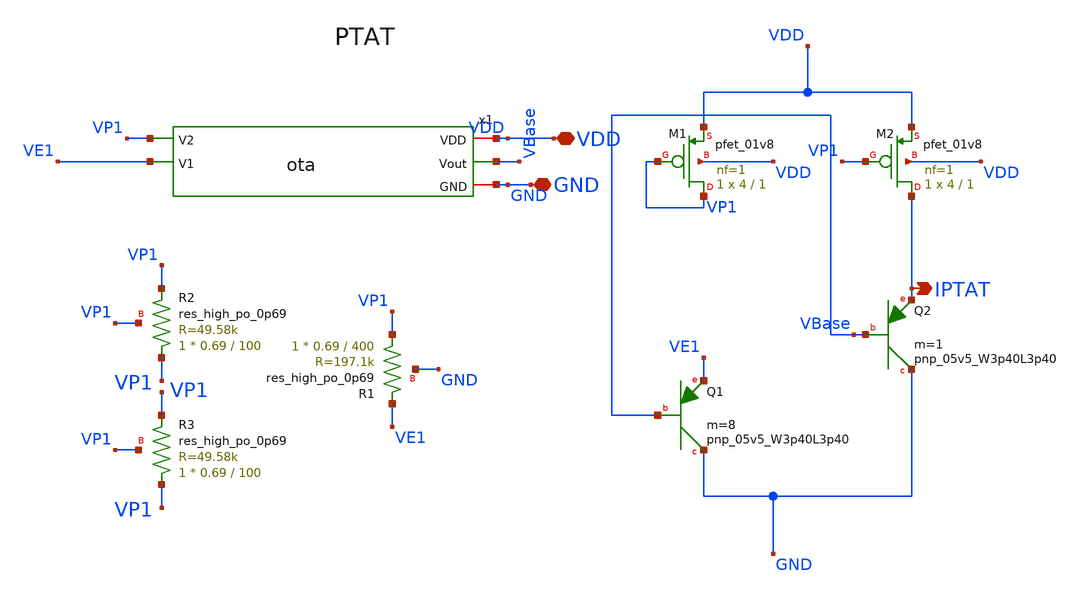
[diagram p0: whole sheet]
** sch_path: subcells/xschem/ptat.sch
**.subckt ptat VDD GND IPTAT
*.iopin VDD
*.iopin GND
*.opin IPTAT
XM1 VP1 VP1 VDD VDD sky130_fd_pr__pfet_01v8 L=1 W=4 nf=1 ad='int((1 + 1)/2) * 4 / 1 * 0.29' as='int((1 + 2)/2) * 4 / 1 * 0.29'
+ pd='2*int((1 + 1)/2) * (4 / 1 + 0.29)' ps='2*int((1 + 2)/2) * (4 / 1 + 0.29)' nrd='0.29 / 4 ' nrs='0.29 / 4 '
+ sa=0 sb=0 sd=0 mult=1 m=1
XM2 IPTAT VP1 VDD VDD sky130_fd_pr__pfet_01v8 L=1 W=4 nf=1 ad='int((1 + 1)/2) * 4 / 1 * 0.29' as='int((1 + 2)/2) * 4 / 1 * 0.29'
+ pd='2*int((1 + 1)/2) * (4 / 1 + 0.29)' ps='2*int((1 + 2)/2) * (4 / 1 + 0.29)' nrd='0.29 / 4 ' nrs='0.29 / 4 '
+ sa=0 sb=0 sd=0 mult=1 m=1
XR1 VP1 VE1 GND sky130_fd_pr__res_high_po_0p69 L=400 mult=1 m=1
x1 VDD VP1 VE1 VBase GND ota
XQ1 GND VBase VE1 sky130_fd_pr__pnp_05v5_W3p40L3p40 m=8
XQ2 GND VBase IPTAT sky130_fd_pr__pnp_05v5_W3p40L3p40 m=1
XR2 VP1 VP1 VP1 sky130_fd_pr__res_high_po_0p69 L=100 mult=1 m=1
XR3 VP1 VP1 VP1 sky130_fd_pr__res_high_po_0p69 L=100 mult=1 m=1
**.ends
.end
